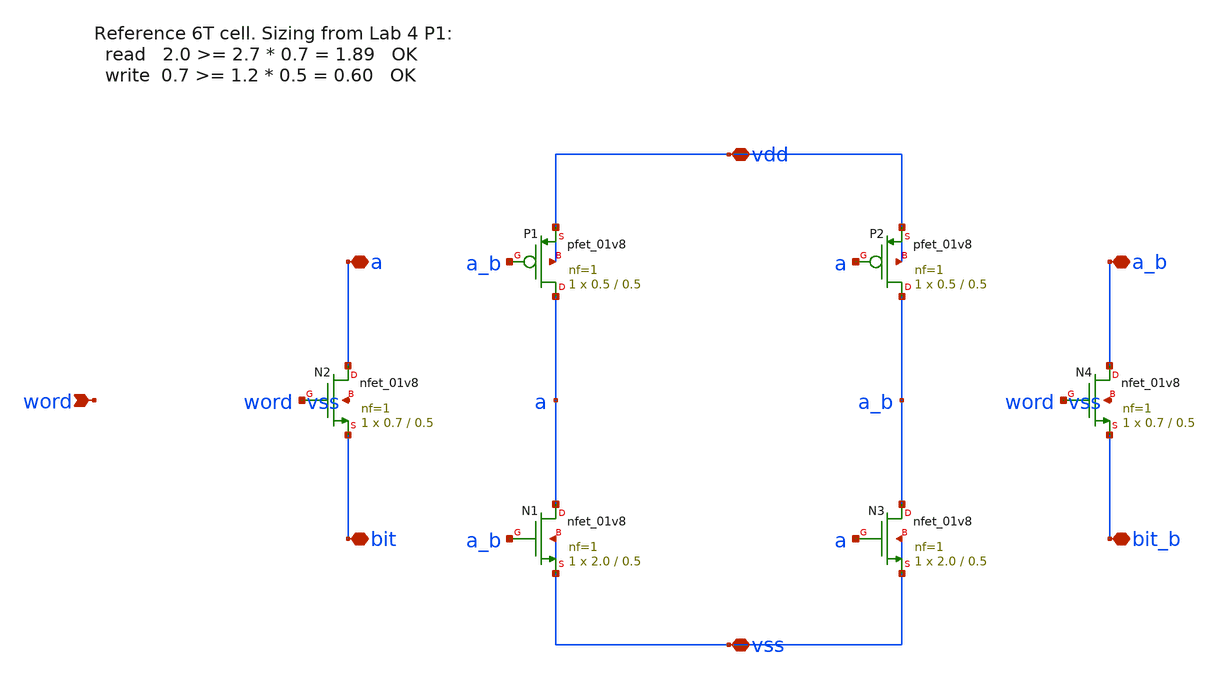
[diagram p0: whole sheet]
** sch_path: instructors/lab4/xschem/dut_sram6t.sch
**.subckt dut_sram6t bit bit_b word a a_b vdd vss
*.iopin bit
*.iopin bit_b
*.ipin word
*.iopin a
*.iopin a_b
*.iopin vdd
*.iopin vss
XP1 a a_b vdd vdd sky130_fd_pr__pfet_01v8 L=0.5 W=0.5 nf=1 ad='int((nf+1)/2) * W/nf * 0.29' as='int((nf+2)/2) * W/nf * 0.29'
+ pd='2*int((nf+1)/2) * (W/nf + 0.29)' ps='2*int((nf+2)/2) * (W/nf + 0.29)' nrd='0.29 / W' nrs='0.29 / W'
+ sa=0 sb=0 sd=0 mult=1 m=1
XN1 a a_b vss vss sky130_fd_pr__nfet_01v8 L=0.5 W=2.0 nf=1 ad='int((1 + 1)/2) * 2.0 / 1 * 0.29' as='int((1 + 2)/2) * 2.0 / 1 * 0.29'
+ pd='2*int((1 + 1)/2) * (2.0 / 1 + 0.29)' ps='2*int((1 + 2)/2) * (2.0 / 1 + 0.29)' nrd='0.29 / 2.0 ' nrs='0.29 / 2.0 '
+ sa=0 sb=0 sd=0 mult=1 m=1
XP2 a_b a vdd vdd sky130_fd_pr__pfet_01v8 L=0.5 W=0.5 nf=1 ad='int((nf+1)/2) * W/nf * 0.29' as='int((nf+2)/2) * W/nf * 0.29'
+ pd='2*int((nf+1)/2) * (W/nf + 0.29)' ps='2*int((nf+2)/2) * (W/nf + 0.29)' nrd='0.29 / W' nrs='0.29 / W'
+ sa=0 sb=0 sd=0 mult=1 m=1
XN3 a_b a vss vss sky130_fd_pr__nfet_01v8 L=0.5 W=2.0 nf=1 ad='int((1 + 1)/2) * 2.0 / 1 * 0.29' as='int((1 + 2)/2) * 2.0 / 1 * 0.29'
+ pd='2*int((1 + 1)/2) * (2.0 / 1 + 0.29)' ps='2*int((1 + 2)/2) * (2.0 / 1 + 0.29)' nrd='0.29 / 2.0 ' nrs='0.29 / 2.0 '
+ sa=0 sb=0 sd=0 mult=1 m=1
XN2 a word bit vss sky130_fd_pr__nfet_01v8 L=0.5 W=0.7 nf=1 ad='int((1 + 1)/2) * 0.7 / 1 * 0.29' as='int((1 + 2)/2) * 0.7 / 1 * 0.29'
+ pd='2*int((1 + 1)/2) * (0.7 / 1 + 0.29)' ps='2*int((1 + 2)/2) * (0.7 / 1 + 0.29)' nrd='0.29 / 0.7 ' nrs='0.29 / 0.7 '
+ sa=0 sb=0 sd=0 mult=1 m=1
XN4 a_b word bit_b vss sky130_fd_pr__nfet_01v8 L=0.5 W=0.7 nf=1 ad='int((1 + 1)/2) * 0.7 / 1 * 0.29'
+ as='int((1 + 2)/2) * 0.7 / 1 * 0.29' pd='2*int((1 + 1)/2) * (0.7 / 1 + 0.29)' ps='2*int((1 + 2)/2) * (0.7 / 1 + 0.29)'
+ nrd='0.29 / 0.7 ' nrs='0.29 / 0.7 ' sa=0 sb=0 sd=0 mult=1 m=1
**.ends
.end
